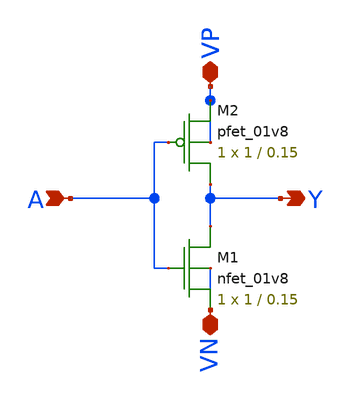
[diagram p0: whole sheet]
** sch_path: Miniproject1/inverter_vtc.sch
**.subckt inverter_vtc A VP VP VN Y
*.ipin A
*.iopin VP
*.iopin VP
*.iopin VN
*.opin Y
XM2 Y A VP VP sky130_fd_pr__pfet_01v8 L=0.15 W=1 nf=1 ad='int((nf+1)/2) * W/nf * 0.29' as='int((nf+2)/2) * W/nf * 0.29'
+ pd='2*int((nf+1)/2) * (W/nf + 0.29)' ps='2*int((nf+2)/2) * (W/nf + 0.29)' nrd='0.29 / W' nrs='0.29 / W'
+ sa=0 sb=0 sd=0 mult=1 m=1
XM1 Y A VN VN sky130_fd_pr__nfet_01v8 L=0.15 W=1 nf=1 ad='int((nf+1)/2) * W/nf * 0.29' as='int((nf+2)/2) * W/nf * 0.29'
+ pd='2*int((nf+1)/2) * (W/nf + 0.29)' ps='2*int((nf+2)/2) * (W/nf + 0.29)' nrd='0.29 / W' nrs='0.29 / W'
+ sa=0 sb=0 sd=0 mult=1 m=1
**.ends
.end
